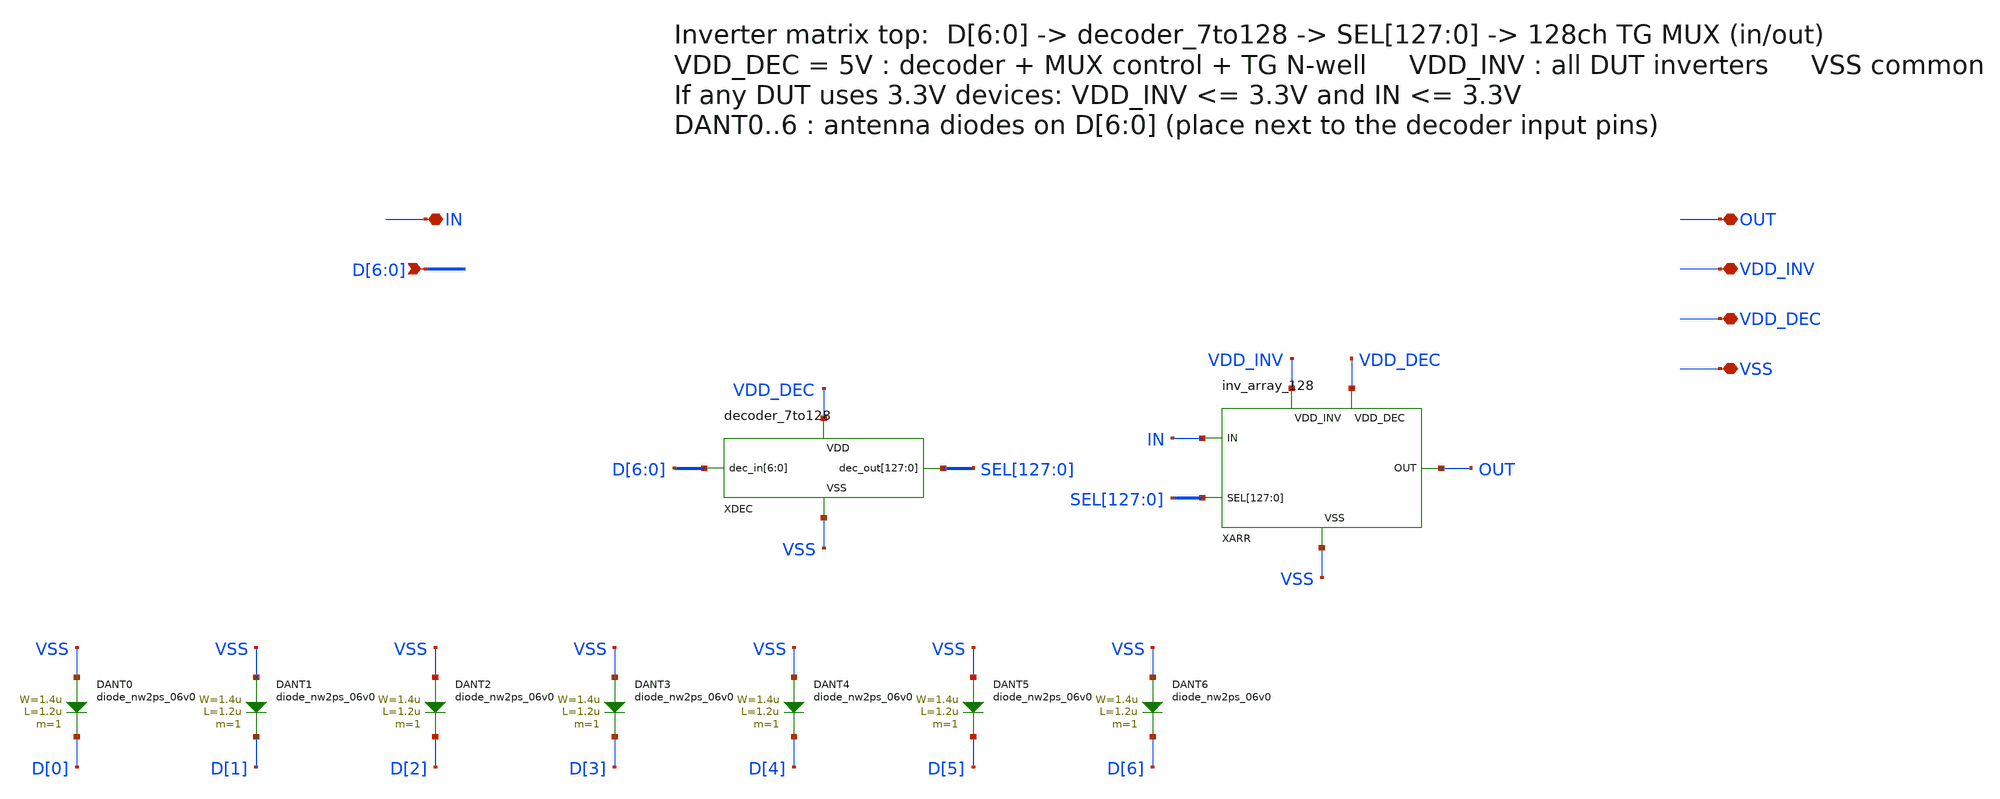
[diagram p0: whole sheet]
** sch_path: inverter_matrix/inv_matrix_top.sch
**.subckt inv_matrix_top IN D[6],D[5],D[4],D[3],D[2],D[1],D[0] OUT VDD_INV VDD_DEC VSS
*.iopin IN
*.ipin D[6],D[5],D[4],D[3],D[2],D[1],D[0]
*.iopin OUT
*.iopin VDD_INV
*.iopin VDD_DEC
*.iopin VSS
XDEC VDD_DEC VSS D[6] D[5] D[4] D[3] D[2] D[1] D[0] SEL[127] SEL[126] SEL[125] SEL[124] SEL[123]
+ SEL[122] SEL[121] SEL[120] SEL[119] SEL[118] SEL[117] SEL[116] SEL[115] SEL[114] SEL[113] SEL[112] SEL[111]
+ SEL[110] SEL[109] SEL[108] SEL[107] SEL[106] SEL[105] SEL[104] SEL[103] SEL[102] SEL[101] SEL[100] SEL[99]
+ SEL[98] SEL[97] SEL[96] SEL[95] SEL[94] SEL[93] SEL[92] SEL[91] SEL[90] SEL[89] SEL[88] SEL[87] SEL[86]
+ SEL[85] SEL[84] SEL[83] SEL[82] SEL[81] SEL[80] SEL[79] SEL[78] SEL[77] SEL[76] SEL[75] SEL[74] SEL[73]
+ SEL[72] SEL[71] SEL[70] SEL[69] SEL[68] SEL[67] SEL[66] SEL[65] SEL[64] SEL[63] SEL[62] SEL[61] SEL[60]
+ SEL[59] SEL[58] SEL[57] SEL[56] SEL[55] SEL[54] SEL[53] SEL[52] SEL[51] SEL[50] SEL[49] SEL[48] SEL[47]
+ SEL[46] SEL[45] SEL[44] SEL[43] SEL[42] SEL[41] SEL[40] SEL[39] SEL[38] SEL[37] SEL[36] SEL[35] SEL[34]
+ SEL[33] SEL[32] SEL[31] SEL[30] SEL[29] SEL[28] SEL[27] SEL[26] SEL[25] SEL[24] SEL[23] SEL[22] SEL[21]
+ SEL[20] SEL[19] SEL[18] SEL[17] SEL[16] SEL[15] SEL[14] SEL[13] SEL[12] SEL[11] SEL[10] SEL[9] SEL[8]
+ SEL[7] SEL[6] SEL[5] SEL[4] SEL[3] SEL[2] SEL[1] SEL[0] decoder_7to128_xs
XARR IN SEL[127] SEL[126] SEL[125] SEL[124] SEL[123] SEL[122] SEL[121] SEL[120] SEL[119] SEL[118]
+ SEL[117] SEL[116] SEL[115] SEL[114] SEL[113] SEL[112] SEL[111] SEL[110] SEL[109] SEL[108] SEL[107] SEL[106]
+ SEL[105] SEL[104] SEL[103] SEL[102] SEL[101] SEL[100] SEL[99] SEL[98] SEL[97] SEL[96] SEL[95] SEL[94]
+ SEL[93] SEL[92] SEL[91] SEL[90] SEL[89] SEL[88] SEL[87] SEL[86] SEL[85] SEL[84] SEL[83] SEL[82] SEL[81]
+ SEL[80] SEL[79] SEL[78] SEL[77] SEL[76] SEL[75] SEL[74] SEL[73] SEL[72] SEL[71] SEL[70] SEL[69] SEL[68]
+ SEL[67] SEL[66] SEL[65] SEL[64] SEL[63] SEL[62] SEL[61] SEL[60] SEL[59] SEL[58] SEL[57] SEL[56] SEL[55]
+ SEL[54] SEL[53] SEL[52] SEL[51] SEL[50] SEL[49] SEL[48] SEL[47] SEL[46] SEL[45] SEL[44] SEL[43] SEL[42]
+ SEL[41] SEL[40] SEL[39] SEL[38] SEL[37] SEL[36] SEL[35] SEL[34] SEL[33] SEL[32] SEL[31] SEL[30] SEL[29]
+ SEL[28] SEL[27] SEL[26] SEL[25] SEL[24] SEL[23] SEL[22] SEL[21] SEL[20] SEL[19] SEL[18] SEL[17] SEL[16]
+ SEL[15] SEL[14] SEL[13] SEL[12] SEL[11] SEL[10] SEL[9] SEL[8] SEL[7] SEL[6] SEL[5] SEL[4] SEL[3] SEL[2]
+ SEL[1] SEL[0] OUT VDD_INV VDD_DEC VSS inv_array_128
DANT0 VSS D[0] diode_nw2ps_06v0 area='1.4u * 1.2u ' pj='2*1.4u + 2*1.2u ' m=1
DANT1 VSS D[1] diode_nw2ps_06v0 area='1.4u * 1.2u ' pj='2*1.4u + 2*1.2u ' m=1
DANT2 VSS D[2] diode_nw2ps_06v0 area='1.4u * 1.2u ' pj='2*1.4u + 2*1.2u ' m=1
DANT3 VSS D[3] diode_nw2ps_06v0 area='1.4u * 1.2u ' pj='2*1.4u + 2*1.2u ' m=1
DANT4 VSS D[4] diode_nw2ps_06v0 area='1.4u * 1.2u ' pj='2*1.4u + 2*1.2u ' m=1
DANT5 VSS D[5] diode_nw2ps_06v0 area='1.4u * 1.2u ' pj='2*1.4u + 2*1.2u ' m=1
DANT6 VSS D[6] diode_nw2ps_06v0 area='1.4u * 1.2u ' pj='2*1.4u + 2*1.2u ' m=1
**.ends
.end
